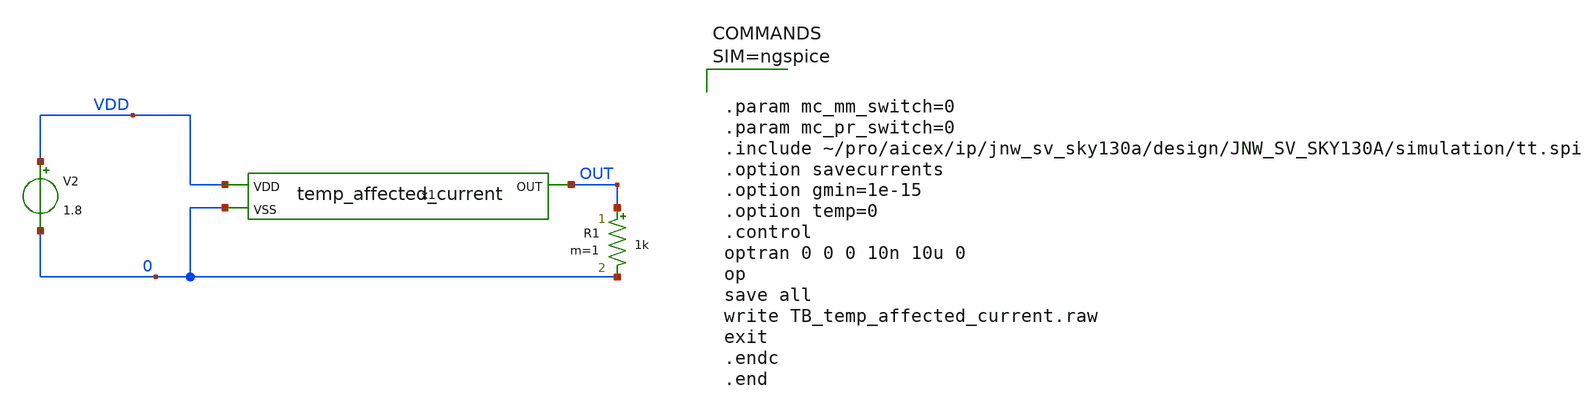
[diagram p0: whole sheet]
** sch_path: design/JNW_GR06_SKY130A/TB_temp_affected_current.sch
**.subckt TB_temp_affected_current
x1 VDD OUT 0 temp_affected_current
V2 VDD 0 1.8
R1 OUT 0 1k m=1
**** begin user architecture code



.param mc_mm_switch=0
.param mc_pr_switch=0
.include ~/pro/aicex/ip/jnw_sv_sky130a/design/JNW_SV_SKY130A/simulation/tt.spi
.option savecurrents
.option gmin=1e-15
.option temp=0
.control
optran 0 0 0 10n 10u 0
op
save all
write TB_temp_affected_current.raw
exit
.endc
.end



**** end user architecture code
**.ends
.end
